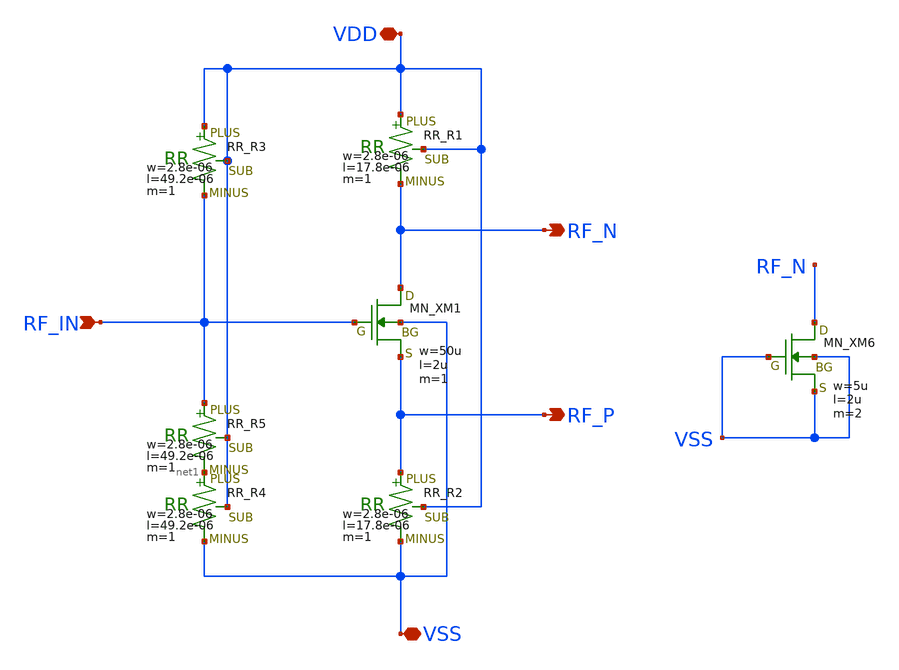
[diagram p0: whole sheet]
** sch_path: member_project/MIXER/noritsuna/xschem/single_to_diff_RF.sch
**.subckt single_to_diff_RF VDD VSS RF_N RF_P RF_IN
*.iopin VDD
*.iopin VSS
*.opin RF_N
*.opin RF_P
*.ipin RF_IN
XXM1 RF_N RF_IN RF_P VSS NMOS w=50u l=2u nrd=0 nrs=0 m=1
XR1 VDD RF_N VDD F_RR w=2.8e-06 l=17.8e-06 R=5e+03 tc1=0 tc2=0 m=1
XR2 RF_P VSS VDD F_RR w=2.8e-06 l=17.8e-06 R=5e+03 tc1=0 tc2=0 m=1
XR3 VDD RF_IN VDD F_RR w=2.8e-06 l=49.2e-06 R=20e+03 tc1=0 tc2=0 m=1
XR4 net1 VSS VDD F_RR w=2.8e-06 l=49.2e-06 R=40e+03 tc1=0 tc2=0 m=1
XXM6 RF_N VSS VSS VSS NMOS w=5u l=2u nrd=0 nrs=0 m=2
XR5 RF_IN net1 VDD F_RR w=2.8e-06 l=49.2e-06 R=40e+03 tc1=0 tc2=0 m=1
**.ends
.end
